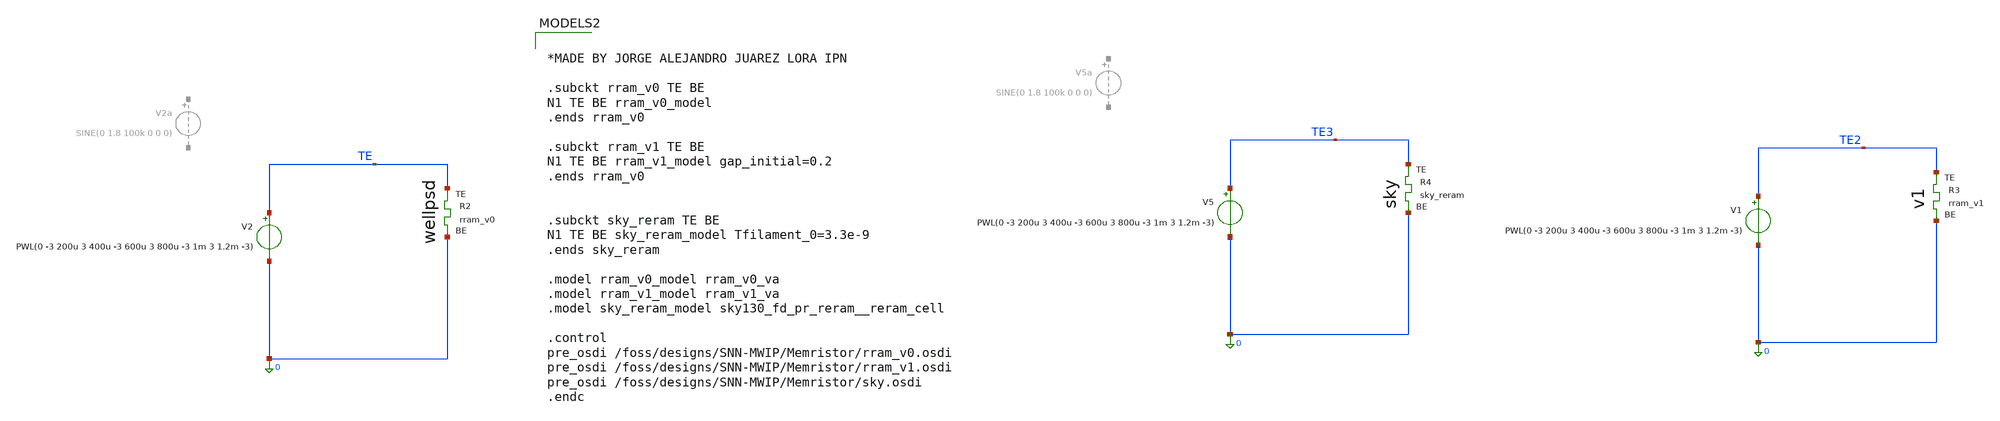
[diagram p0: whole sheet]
** sch_path: Memristor/tb_liss_rram_v0.sch
**.subckt tb_liss_rram_v0
V2 TE 0 PWL(0 -3 200u 3 400u -3 600u 3 800u -3 1m 3 1.2m -3)
XR2 TE 0 rram_v0
XR4 TE3 0 sky_reram
V5 TE3 0 PWL(0 -3 200u 3 400u -3 600u 3 800u -3 1m 3 1.2m -3)
V1 TE2 0 PWL(0 -3 200u 3 400u -3 600u 3 800u -3 1m 3 1.2m -3)
XR3 TE2 0 rram_v1
**** begin user architecture code


.options num_threads=8
.tran 20n 1.2m uic
.control
	save all
	run
	write tb_liss_rram_v0.raw
.endc




*MADE BY JORGE ALEJANDRO JUAREZ LORA IPN

.subckt rram_v0 TE BE
N1 TE BE rram_v0_model
.ends rram_v0

.subckt rram_v1 TE BE
N1 TE BE rram_v1_model gap_initial=0.2
.ends rram_v0


.subckt sky_reram TE BE
N1 TE BE sky_reram_model Tfilament_0=3.3e-9
.ends sky_reram

.model rram_v0_model rram_v0_va
.model rram_v1_model rram_v1_va
.model sky_reram_model sky130_fd_pr_reram__reram_cell

.control
pre_osdi /foss/designs/SNN-MWIP/Memristor/rram_v0.osdi
pre_osdi /foss/designs/SNN-MWIP/Memristor/rram_v1.osdi
pre_osdi /foss/designs/SNN-MWIP/Memristor/sky.osdi
.endc

**** end user architecture code
**.ends
.end
